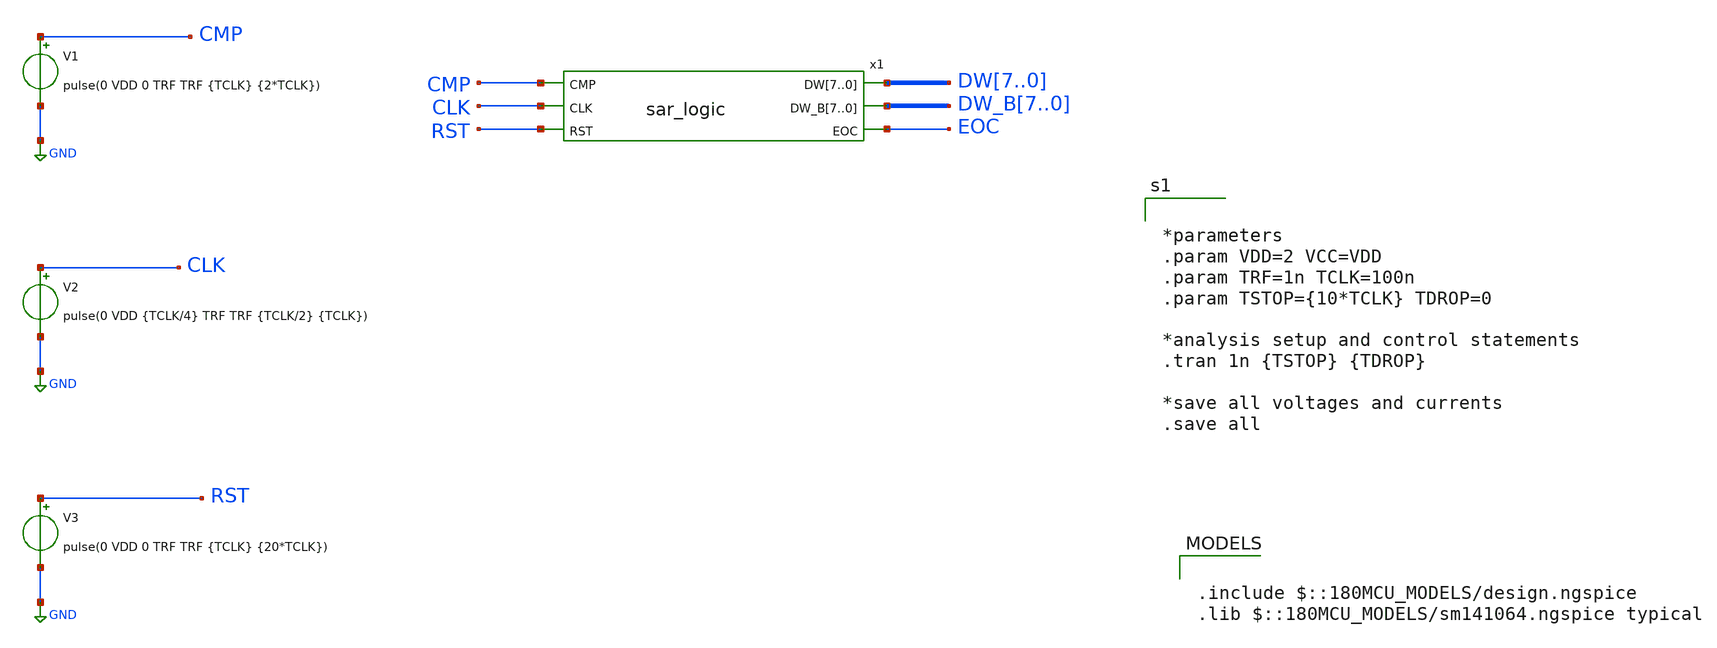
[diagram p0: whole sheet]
** sch_path: XSCHEM Files/sar_logic_tb.sch
**.subckt sar_logic_tb
V1 CMP GND pulse(0 VDD 0 TRF TRF {TCLK} {2*TCLK})
V2 CLK GND pulse(0 VDD {TCLK/4} TRF TRF {TCLK/2} {TCLK})
V3 RST GND pulse(0 VDD 0 TRF TRF {TCLK} {20*TCLK})
x1 CMP CLK RST DW7 DW6 DW5 DW4 DW3 DW2 DW1 DW0 DW_B7 DW_B6 DW_B5 DW_B4 DW_B3 DW_B2 DW_B1 DW_B0 EOC
+ sar_logic
**** begin user architecture code


*parameters
.param VDD=2 VCC=VDD
.param TRF=1n TCLK=100n
.param TSTOP={10*TCLK} TDROP=0

*analysis setup and control statements
.tran 1n {TSTOP} {TDROP}

*save all voltages and currents
.save all



.include $::180MCU_MODELS/design.ngspice
.lib $::180MCU_MODELS/sm141064.ngspice typical

**** end user architecture code
**.ends

* expanding   symbol:  /home/tare/Desktop/sar_adc/sar_logic.sym # of pins=6
** sym_path: XSCHEM Files/sar_logic.sym
** sch_path: XSCHEM Files/sar_logic.sch
.subckt sar_logic CMP CLK RST DW7 DW6 DW5 DW4 DW3 DW2 DW1 DW0 DW_B7 DW_B6 DW_B5 DW_B4 DW_B3 DW_B2
+ DW_B1 DW_B0 EOC
*.ipin CMP
*.opin DW7,DW6,DW5,DW4,DW3,DW2,DW1,DW0
*.ipin CLK
*.ipin RST
*.opin DW_B7,DW_B6,DW_B5,DW_B4,DW_B3,DW_B2,DW_B1,DW_B0
*.opin EOC
**** begin user architecture code


V1 VLOW 0 0


**** end user architecture code
xRING_CNT8 VLOW CLK RST VLOW QCNT8 Q_B8 dff
xRING_CNT7 QCNT8 CLK VLOW RST QCNT7 Q_B7 dff
xRING_CNT6 QCNT7 CLK VLOW RST QCNT6 Q_B6 dff
xRING_CNT5 QCNT6 CLK VLOW RST QCNT5 Q_B5 dff
xRING_CNT4 QCNT5 CLK VLOW RST QCNT4 Q_B4 dff
xRING_CNT3 QCNT4 CLK VLOW RST QCNT3 Q_B3 dff
xRING_CNT2 QCNT3 CLK VLOW RST QCNT2 Q_B2 dff
xRING_CNT1 QCNT2 CLK VLOW RST QCNT1 Q_B1 dff
xRING_CNT0 QCNT1 CLK VLOW RST QCNT0 Q_B0 dff
xCODE_REG7 CMP DW6 QCNT8 VLOW DW7 DW_B7 dff
xCODE_REG6 CMP DW5 QCNT7 RST DW6 DW_B6 dff
xCODE_REG5 CMP DW4 QCNT6 RST DW5 DW_B5 dff
xCODE_REG4 CMP DW3 QCNT5 RST DW4 DW_B4 dff
xCODE_REG3 CMP DW2 QCNT4 RST DW3 DW_B3 dff
xCODE_REG2 CMP DW1 QCNT3 RST DW2 DW_B2 dff
xCODE_REG1 CMP DW0 QCNT2 RST DW1 DW_B1 dff
xCODE_REG0 CMP EOC QCNT1 RST DW0 DW_B0 dff
x3 VLOW VLOW QCNT0 RST EOC net1 dff
.ends


* expanding   symbol:  /home/tare/Desktop/sar_adc/dff.sym # of pins=6
** sym_path: XSCHEM Files/dff.sym
** sch_path: XSCHEM Files/dff.sch
.subckt dff D CLK SET RESET Q QB
*.ipin D
*.opin Q
*.ipin CLK
*.ipin SET
*.ipin RESET
*.opin QB
**** begin user architecture code


*nor model
a1 D CLK SET RESET OUT OUTI my_dff
.model my_dff d_dff(clk_delay = 13.0e-9 set_delay = 25.0e-9                    reset_delay = 27.0e-9
+ ic = 2 rise_delay = 10.0e-9                    fall_delay = 3e-9)

*force netlisting of digital outputs
v1 OUT Q 0
v2 OUTI QB 1


**** end user architecture code
.ends

.GLOBAL GND
.end
